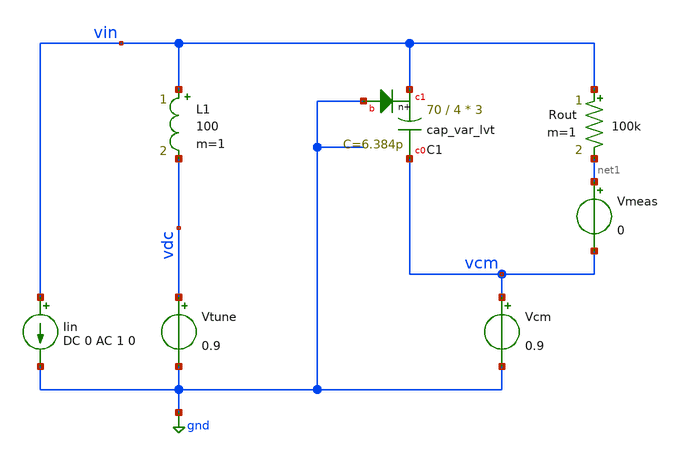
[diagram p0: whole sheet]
** sch_path: pll/pll_vco/simulation/varactor_tb.sch
**.subckt varactor_tb
Iin vin gnd DC 0 AC 1 0
Vtune vdc gnd 0.9
Vcm vcm gnd 0.9
Rout vin net1 100k m=1
Vmeas net1 vcm 0
L1 vin vdc 100 m=1
XC1 vcm vin gnd sky130_fd_pr__cap_var_lvt W=70 L=4 VM=3 m=3
**** begin user architecture code



.option savecurrents

* Settings for PSS osciallator
.option reltol=1e-5
.option vntol=3e-8
.option abstol=1e-13
*.option chgtol=1e-12
.option trtol=10
.option method=gear


.control
* Main Amplifier
** Main Core OP params
*save i(@m.x1.xm1.msky130_fd_pr__nfet_01v8[id])
*save @m.x1.xm1.msky130_fd_pr__nfet_01v8[gm]
*save v(@m.x1.xm1.msky130_fd_pr__nfet_01v8[vds])
*save v(@m.x1.xm1.msky130_fd_pr__nfet_01v8[vgs])
*save v(@m.x1.xm1.msky130_fd_pr__nfet_01v8[vth])
*save v(@m.x1.xm1.msky130_fd_pr__nfet_01v8[vdsat])


* #################################################################
* #
* #                         OPERATING POINT
* #
* #################################################################
reset
setplot const
save all

op
set filetype=binary
write varactor_tb.raw all


* #################################################################
* #
* #                         AC RESPONSE
* #
* #################################################################
reset
setplot const
save all

ac dec 100 100k 10G
set filetype=ascii
write varactor_tb_ac.raw all

* Plot AC
plot db(vmeas#branch)

* Calculate 3dbfreq
let gain=db(vmeas#branch)
meas ac f3db WHEN gain=-3 FALL=1
let f3db_mhz=f3db/1e6
set f3db_mhz=$&f3db_mhz
echo Corner Frequency: $f3db_mhz MHz

* Calculate capacitance
let cvar=(1/(2*pi*100e3*f3db))
let cvar_pf=cvar*1e12
set cvar=$&cvar
set cvar_pf=$&cvar
echo Capacitance: $cvar_pf pF

reset
setplot const
save all

let run = 0
let vtune_start = 0.0
let vtune_stop = 2.0
let vtune_step = 0.01
let vtune_val = vtune_start
let vtune_length = (vtune_stop-vtune_start)/vtune_step

set curplot = new
set ac_sweep_plot = $curplot

let cvar_vect = vector(vtune_length)
let vtune_sweep = vector(vtune_length)

while vtune_val le vtune_stop
	* Print run variables
	set run = $&run
	set run_total = $&vtune_length
	set vtune_val = $&vtune_val
	echo #############################################################
	echo Run: $run / $run_total for vtune: $vtune_val V
	echo #############################################################

	* Run AC
	reset

	* Set sweep variable
	alter Vtune=vtune_val

	save all
	ac dec 100 100k 10G
	set filetype=ascii
	set simfilename =  {varactor_tb_ac_sweep_}{$&run}{.raw}
	write $simfilename all

	* Calculate 3dbfreq
	let gain=db(vmeas#branch)
	meas ac f3db WHEN gain=-3 FALL=1
	let f3db_mhz=f3db/1e6
	set f3db_mhz=$&f3db_mhz
	echo Corner Frequency: $f3db_mhz MHz

	* Calculate capacitance
	let cvar=(1/(2*pi*100e3*f3db))
	let cvar_pf=cvar*1e12
	set cvar=$&cvar
	set cvar_pf=$&cvar_pf
	echo Capacitance: $cvar_pf pF

	* Switch to new plot environment
	set dt = $curplot
	setplot $ac_sweep_plot

	* Save values to variable
	let vtune_sweep[$run] = vtune_val
	let cvar_vect[$run] = {$dt}.cvar

	* Switch back to original environment
	setplot $dt

	let vtune_val = vtune_val + vtune_step
	let run = run + 1
end

echo #############################################################
echo Post Process data
echo #############################################################

* Set environment
setplot $ac_sweep_plot

* Calculate capacitor ratio
let c_min=cvar_vect[0]*1e12
set c_min=$&c_min
let c_max=cvar_vect[vtune_length-1]*1e12
set c_max=$&c_max
let c_ratio=c_max/c_min
set c_ratio=$&c_ratio
echo Capacitance ratio: $c_max pF / $c_min pF = $c_ratio

* Plot data
plot cvar_vect vs vtune_sweep

let v_var_vect = vtune_sweep-v(op1.vcm)
plot cvar_vect vs v_var_vect

set filetype=ascii
write varactor_tb_ac_sweep.raw all


* #################################################################
* #
* #                 TRANSIENT OSCILATION REGIME
* #
* #################################################################
*reset
*setplot const
*save all

*tran 0.005n 20n uic
*set filetype=ascii
*write varactor_tb_tran.raw all

* Plot internal nodes
*plot v("phi<0>") v("phi<4>")
*plot v("phi<1>") v("phi<5>")

* Plot outputs
*plot v("out<0>")+2 v("out<4>")+2 v("out<1>")+0 v("out<5>")+0 v("out<2>")-2 v("out<6>")-2
*+ v("out<3>")-4 v("out<7>")-4
*plot v("out<0>") v("out<4>")
*plot v("out<1>") v("out<5>")
*plot v("out<2>") v("out<6>")
*plot v("out<3>") v("out<7>")


*rusage
.endc



.options wnflag=1
.include $::SKYWATER_MODELS/cells/nfet_01v8/sky130_fd_pr__nfet_01v8__tt.corner.spice
.include $::SKYWATER_MODELS/cells/nfet_01v8_lvt/sky130_fd_pr__nfet_01v8_lvt__tt.corner.spice
.include $::SKYWATER_MODELS/cells/pfet_01v8/sky130_fd_pr__pfet_01v8__tt.corner.spice
.include $::SKYWATER_MODELS/cells/nfet_03v3_nvt/sky130_fd_pr__nfet_03v3_nvt__tt.corner.spice
.include $::SKYWATER_MODELS/cells/nfet_05v0_nvt/sky130_fd_pr__nfet_05v0_nvt__tt.corner.spice
.include $::SKYWATER_MODELS/cells/esd_nfet_01v8/sky130_fd_pr__esd_nfet_01v8__tt.corner.spice
.include $::SKYWATER_MODELS/cells/pfet_01v8_lvt/sky130_fd_pr__pfet_01v8_lvt__tt.corner.spice
.include $::SKYWATER_MODELS/cells/pfet_01v8_hvt/sky130_fd_pr__pfet_01v8_hvt__tt.corner.spice
.include $::SKYWATER_MODELS/cells/esd_pfet_g5v0d10v5/sky130_fd_pr__esd_pfet_g5v0d10v5__tt.corner.spice
.include $::SKYWATER_MODELS/cells/pfet_g5v0d10v5/sky130_fd_pr__pfet_g5v0d10v5__tt.corner.spice
.include $::SKYWATER_MODELS/cells/pfet_g5v0d16v0/sky130_fd_pr__pfet_g5v0d16v0__tt.corner.spice
.include $::SKYWATER_MODELS/cells/nfet_g5v0d10v5/sky130_fd_pr__nfet_g5v0d10v5__tt.corner.spice
.include $::SKYWATER_MODELS/cells/nfet_g5v0d16v0/sky130_fd_pr__nfet_g5v0d16v0__tt_discrete.corner.spice
.include $::SKYWATER_MODELS/cells/esd_nfet_g5v0d10v5/sky130_fd_pr__esd_nfet_g5v0d10v5__tt.corner.spice
.include $::SKYWATER_MODELS/models/corners/tt/nonfet.spice

.include $::SKYWATER_MODELS/cells/cap_var_hvt/sky130_fd_pr__cap_var_hvt.model.spice

* Mismatch parameters
.include $::SKYWATER_MODELS/cells/nfet_01v8/sky130_fd_pr__nfet_01v8__mismatch.corner.spice
.include $::SKYWATER_MODELS/cells/pfet_01v8/sky130_fd_pr__pfet_01v8__mismatch.corner.spice
.include $::SKYWATER_MODELS/cells/nfet_01v8_lvt/sky130_fd_pr__nfet_01v8_lvt__mismatch.corner.spice
.include $::SKYWATER_MODELS/cells/pfet_01v8_lvt/sky130_fd_pr__pfet_01v8_lvt__mismatch.corner.spice
.include $::SKYWATER_MODELS/cells/pfet_01v8_hvt/sky130_fd_pr__pfet_01v8_hvt__mismatch.corner.spice
.include $::SKYWATER_MODELS/cells/nfet_g5v0d10v5/sky130_fd_pr__nfet_g5v0d10v5__mismatch.corner.spice
.include $::SKYWATER_MODELS/cells/pfet_g5v0d10v5/sky130_fd_pr__pfet_g5v0d10v5__mismatch.corner.spice
.include $::SKYWATER_MODELS/cells/nfet_05v0_nvt/sky130_fd_pr__nfet_05v0_nvt__mismatch.corner.spice
.include $::SKYWATER_MODELS/cells/nfet_03v3_nvt/sky130_fd_pr__nfet_03v3_nvt__mismatch.corner.spice

* Resistor$::SKYWATER_MODELS/Capacitor
.include $::SKYWATER_MODELS/models/r+c/res_typical__cap_typical.spice
.include $::SKYWATER_MODELS/models/r+c/res_typical__cap_typical__lin.spice

* Special cells
.include $::SKYWATER_MODELS/models/corners/tt/specialized_cells.spice

* All models
.include $::SKYWATER_MODELS/models/all.spice

* Corner
.include $::SKYWATER_MODELS/models/corners/tt/rf.spice

* .include $::SKYWATER_STDCELLS/cells/
.include $::SKYWATER_STDCELLS/cells/buf/sky130_fd_sc_hd__buf_1.spice
.include $::SKYWATER_STDCELLS_HS/cells/buf/sky130_fd_sc_hs__buf_1.spice
.include $::SKYWATER_STDCELLS_HS/cells/buf/sky130_fd_sc_hs__buf_16.spice
.include $::SKYWATER_STDCELLS/cells/clkbuf/sky130_fd_sc_hd__clkbuf_1.spice
.include $::SKYWATER_STDCELLS/cells/clkbuf/sky130_fd_sc_hd__clkbuf_2.spice
.include $::SKYWATER_STDCELLS/cells/clkbuf/sky130_fd_sc_hd__clkbuf_4.spice
.include $::SKYWATER_STDCELLS/cells/clkbuf/sky130_fd_sc_hd__clkbuf_8.spice
.include $::SKYWATER_STDCELLS/cells/clkbuf/sky130_fd_sc_hd__clkbuf_16.spice
.include $::SKYWATER_STDCELLS/cells/decap/sky130_fd_sc_hd__decap_3.spice
.include $::SKYWATER_STDCELLS/cells/decap/sky130_fd_sc_hd__decap_4.spice
.include $::SKYWATER_STDCELLS/cells/decap/sky130_fd_sc_hd__decap_8.spice
.include $::SKYWATER_STDCELLS/cells/dfrbp/sky130_fd_sc_hd__dfrbp_1.spice
.include $::SKYWATER_STDCELLS/cells/dfrbp/sky130_fd_sc_hd__dfrbp_2.spice
.include $::SKYWATER_STDCELLS/cells/inv/sky130_fd_sc_hd__inv_1.spice
.include $::SKYWATER_STDCELLS/cells/inv/sky130_fd_sc_hd__inv_2.spice
.include $::SKYWATER_STDCELLS/cells/inv/sky130_fd_sc_hd__inv_4.spice
.include $::SKYWATER_STDCELLS/cells/inv/sky130_fd_sc_hd__inv_8.spice
.include $::SKYWATER_STDCELLS/cells/inv/sky130_fd_sc_hd__inv_16.spice
.include $::SKYWATER_STDCELLS_HS/cells/inv/sky130_fd_sc_hs__inv_1.spice
.include $::SKYWATER_STDCELLS_HS/cells/inv/sky130_fd_sc_hs__inv_2.spice
.include $::SKYWATER_STDCELLS_HS/cells/inv/sky130_fd_sc_hs__inv_4.spice
.include $::SKYWATER_STDCELLS_HS/cells/inv/sky130_fd_sc_hs__inv_8.spice
.include $::SKYWATER_STDCELLS_HS/cells/inv/sky130_fd_sc_hs__inv_16.spice
.include $::SKYWATER_STDCELLS/cells/mux2/sky130_fd_sc_hd__mux2_2.spice
.include $::SKYWATER_STDCELLS/cells/nand2/sky130_fd_sc_hd__nand2_1.spice
.include $::SKYWATER_STDCELLS/cells/tap/sky130_fd_sc_hd__tap_2.spice
.include $::SKYWATER_STDCELLS/cells/tapvpwrvgnd/sky130_fd_sc_hd__tapvpwrvgnd_1.spice

**** end user architecture code
**.ends
.GLOBAL gnd
.end
